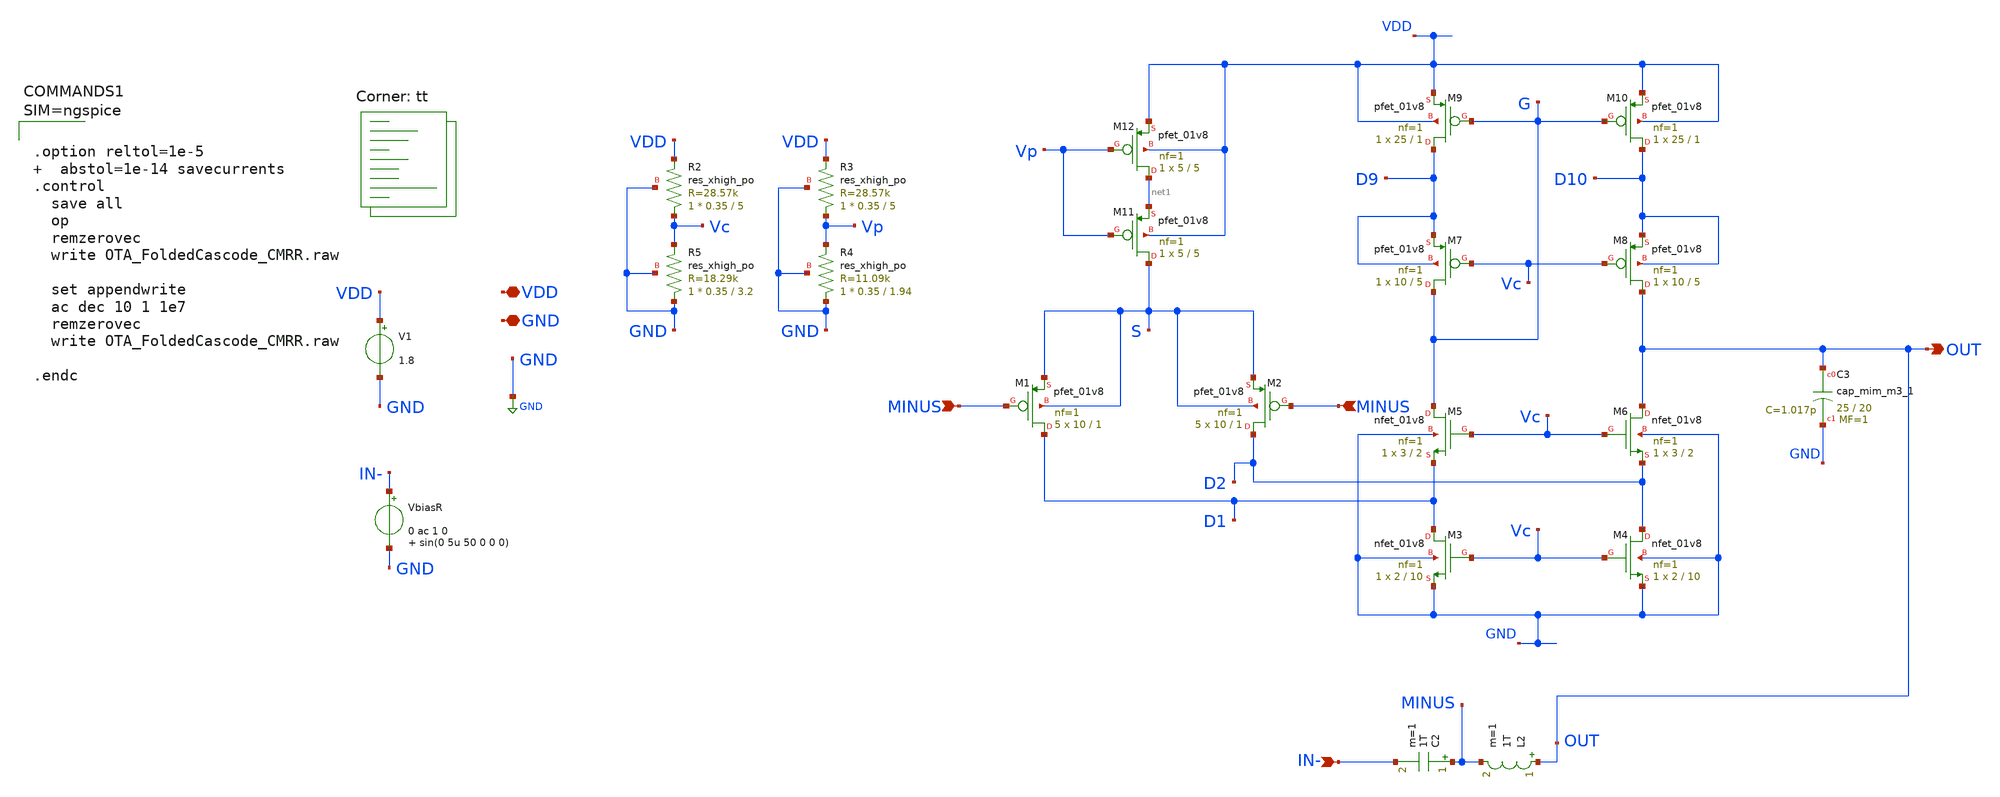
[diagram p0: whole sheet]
** sch_path: xschem/OTA_FoldedCascode_CMRR.sch
**.subckt OTA_FoldedCascode_CMRR VDD GND IN- OUT MINUS MINUS
*.iopin VDD
*.iopin GND
*.ipin IN-
*.opin OUT
*.ipin MINUS
*.ipin MINUS
V1 VDD GND 1.8
VbiasR IN- GND 0 ac 1 0 sin(0 5u 50 0 0 0)
C2 MINUS IN- 1T m=1
L2 OUT MINUS 1T m=1
XC3 OUT GND sky130_fd_pr__cap_mim_m3_1 W=25 L=20 MF=1 m=1
XM1 D1 MINUS S S sky130_fd_pr__pfet_01v8 L=1 W=10 nf=1 ad='int((nf+1)/2) * W/nf * 0.29' as='int((nf+2)/2) * W/nf * 0.29'
+ pd='2*int((nf+1)/2) * (W/nf + 0.29)' ps='2*int((nf+2)/2) * (W/nf + 0.29)' nrd='0.29 / W' nrs='0.29 / W'
+ sa=0 sb=0 sd=0 mult=5 m=5
XM2 D2 MINUS S S sky130_fd_pr__pfet_01v8 L=1 W=10 nf=1 ad='int((nf+1)/2) * W/nf * 0.29' as='int((nf+2)/2) * W/nf * 0.29'
+ pd='2*int((nf+1)/2) * (W/nf + 0.29)' ps='2*int((nf+2)/2) * (W/nf + 0.29)' nrd='0.29 / W' nrs='0.29 / W'
+ sa=0 sb=0 sd=0 mult=5 m=5
XM3 D1 Vc GND GND sky130_fd_pr__nfet_01v8 L=10 W=2 nf=1 ad='int((nf+1)/2) * W/nf * 0.29' as='int((nf+2)/2) * W/nf * 0.29'
+ pd='2*int((nf+1)/2) * (W/nf + 0.29)' ps='2*int((nf+2)/2) * (W/nf + 0.29)' nrd='0.29 / W' nrs='0.29 / W'
+ sa=0 sb=0 sd=0 mult=1 m=1
XM4 D2 Vc GND GND sky130_fd_pr__nfet_01v8 L=10 W=2 nf=1 ad='int((nf+1)/2) * W/nf * 0.29' as='int((nf+2)/2) * W/nf * 0.29'
+ pd='2*int((nf+1)/2) * (W/nf + 0.29)' ps='2*int((nf+2)/2) * (W/nf + 0.29)' nrd='0.29 / W' nrs='0.29 / W'
+ sa=0 sb=0 sd=0 mult=1 m=1
XM5 G Vc D1 GND sky130_fd_pr__nfet_01v8 L=2 W=3 nf=1 ad='int((nf+1)/2) * W/nf * 0.29' as='int((nf+2)/2) * W/nf * 0.29'
+ pd='2*int((nf+1)/2) * (W/nf + 0.29)' ps='2*int((nf+2)/2) * (W/nf + 0.29)' nrd='0.29 / W' nrs='0.29 / W'
+ sa=0 sb=0 sd=0 mult=1 m=1
XM6 OUT Vc D2 GND sky130_fd_pr__nfet_01v8 L=2 W=3 nf=1 ad='int((nf+1)/2) * W/nf * 0.29' as='int((nf+2)/2) * W/nf * 0.29'
+ pd='2*int((nf+1)/2) * (W/nf + 0.29)' ps='2*int((nf+2)/2) * (W/nf + 0.29)' nrd='0.29 / W' nrs='0.29 / W'
+ sa=0 sb=0 sd=0 mult=1 m=1
XM7 G Vc D9 D9 sky130_fd_pr__pfet_01v8 L=5 W=10 nf=1 ad='int((nf+1)/2) * W/nf * 0.29' as='int((nf+2)/2) * W/nf * 0.29'
+ pd='2*int((nf+1)/2) * (W/nf + 0.29)' ps='2*int((nf+2)/2) * (W/nf + 0.29)' nrd='0.29 / W' nrs='0.29 / W'
+ sa=0 sb=0 sd=0 mult=1 m=1
XM8 OUT Vc D10 D10 sky130_fd_pr__pfet_01v8 L=5 W=10 nf=1 ad='int((nf+1)/2) * W/nf * 0.29' as='int((nf+2)/2) * W/nf * 0.29'
+ pd='2*int((nf+1)/2) * (W/nf + 0.29)' ps='2*int((nf+2)/2) * (W/nf + 0.29)' nrd='0.29 / W' nrs='0.29 / W'
+ sa=0 sb=0 sd=0 mult=1 m=1
XM9 D9 G VDD VDD sky130_fd_pr__pfet_01v8 L=1 W=25 nf=1 ad='int((nf+1)/2) * W/nf * 0.29' as='int((nf+2)/2) * W/nf * 0.29'
+ pd='2*int((nf+1)/2) * (W/nf + 0.29)' ps='2*int((nf+2)/2) * (W/nf + 0.29)' nrd='0.29 / W' nrs='0.29 / W'
+ sa=0 sb=0 sd=0 mult=1 m=1
XM10 D10 G VDD VDD sky130_fd_pr__pfet_01v8 L=1 W=25 nf=1 ad='int((nf+1)/2) * W/nf * 0.29' as='int((nf+2)/2) * W/nf * 0.29'
+ pd='2*int((nf+1)/2) * (W/nf + 0.29)' ps='2*int((nf+2)/2) * (W/nf + 0.29)' nrd='0.29 / W' nrs='0.29 / W'
+ sa=0 sb=0 sd=0 mult=1 m=1
XM11 S Vp net1 VDD sky130_fd_pr__pfet_01v8 L=5 W=5 nf=1 ad='int((nf+1)/2) * W/nf * 0.29' as='int((nf+2)/2) * W/nf * 0.29'
+ pd='2*int((nf+1)/2) * (W/nf + 0.29)' ps='2*int((nf+2)/2) * (W/nf + 0.29)' nrd='0.29 / W' nrs='0.29 / W'
+ sa=0 sb=0 sd=0 mult=1 m=1
XM12 net1 Vp VDD VDD sky130_fd_pr__pfet_01v8 L=5 W=5 nf=1 ad='int((nf+1)/2) * W/nf * 0.29' as='int((nf+2)/2) * W/nf * 0.29'
+ pd='2*int((nf+1)/2) * (W/nf + 0.29)' ps='2*int((nf+2)/2) * (W/nf + 0.29)' nrd='0.29 / W' nrs='0.29 / W'
+ sa=0 sb=0 sd=0 mult=1 m=1
XR5 GND Vc GND sky130_fd_pr__res_xhigh_po W=0.35 L=3.2 mult=1 m=1
XR2 Vc VDD GND sky130_fd_pr__res_xhigh_po W=0.35 L=5 mult=1 m=1
XR3 Vp VDD GND sky130_fd_pr__res_xhigh_po W=0.35 L=5 mult=1 m=1
XR4 GND Vp GND sky130_fd_pr__res_xhigh_po W=0.35 L=1.94 mult=1 m=1
**** begin user architecture code



.option reltol=1e-5   abstol=1e-14 savecurrents
.control
  save all
  op
  remzerovec
  write OTA_FoldedCascode_CMRR.raw

  set appendwrite
  ac dec 10 1 1e7
  remzerovec
  write OTA_FoldedCascode_CMRR.raw

.endc



.lib $::SKYWATER_MODELS/sky130.lib.spice tt
**** end user architecture code
**.ends
.GLOBAL GND
.end
